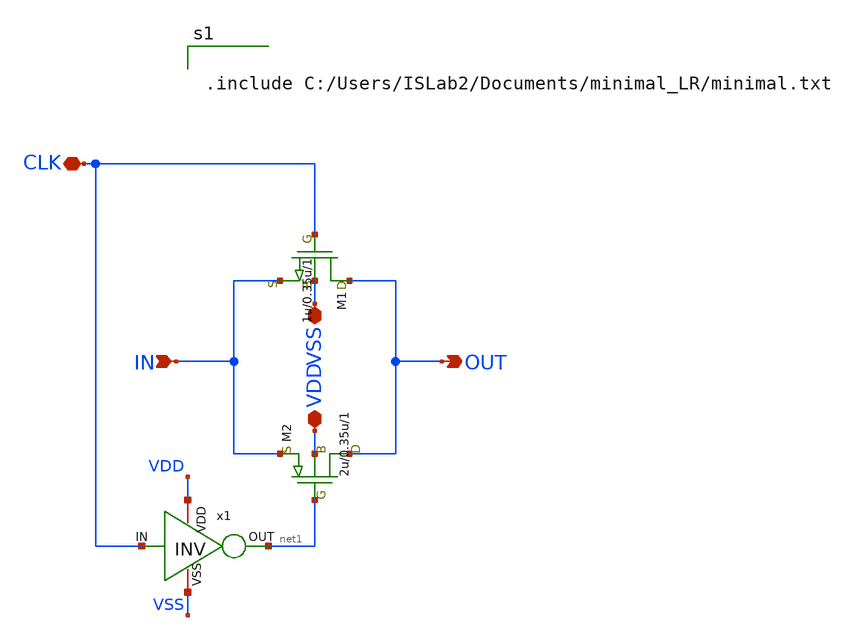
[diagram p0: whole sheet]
** sch_path: CMOSSW.sch
**.subckt CMOSSW IN VDD VSS OUT CLK
*.ipin IN
*.iopin VDD
*.iopin VSS
*.opin OUT
*.iopin CLK
M1 OUT CLK IN VSS nch w=1u l=0.35u as=0 ps=0 ad=0 pd=0 m=1
M2 OUT net1 IN VDD pch w=2u l=0.35u as=0 ps=0 ad=0 pd=0 m=1
x1 VDD net1 CLK VSS INV
**** begin user architecture code


.include C:/Users/ISLab2/Documents/minimal_LR/minimal.txt

**** end user architecture code
**.ends

* expanding   symbol:  C:/Users/ISLab2/Documents/minimal_LR/INV.sym # of pins=4
** sym_path: INV.sym
** sch_path: INV.sch
.subckt INV VDD OUT IN VSS
*.opin OUT
*.ipin IN
*.iopin VDD
*.iopin VSS
M2 OUT IN VDD VDD pch w=10u l=0.35u as=0 ps=0 ad=0 pd=0 m=1
M1 OUT IN VSS VSS nch w=5u l=0.35u as=0 ps=0 ad=0 pd=0 m=1
**** begin user architecture code


.include C:/Users/ISLab2/Documents/minimal_LR/minimal.txt

**** end user architecture code
.ends

.end
